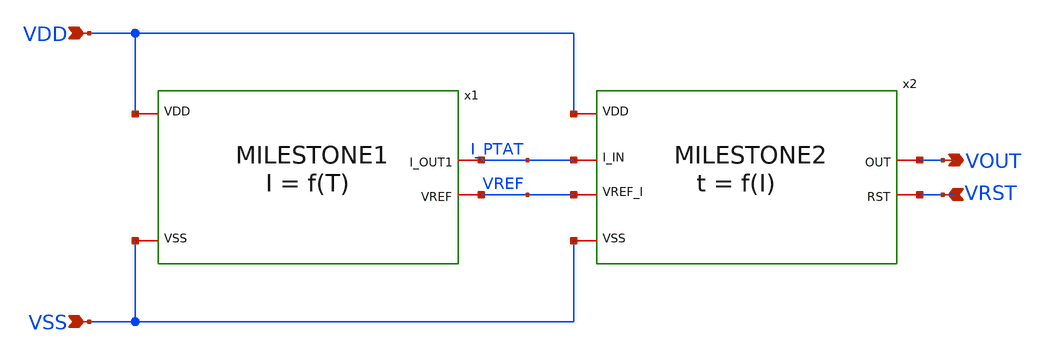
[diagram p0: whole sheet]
** sch_path: design/CNR_GR03_SKY130NM/TOPLEVEL.sch
**.subckt TOPLEVEL VDD VSS VRST VOUT
*.ipin VDD
*.ipin VSS
*.ipin VRST
*.opin VOUT
x1 VDD I_PTAT VREF VSS MILESTONE1
x2 I_PTAT VREF VOUT VDD VRST VSS MILESTONE2
**.ends
.end
